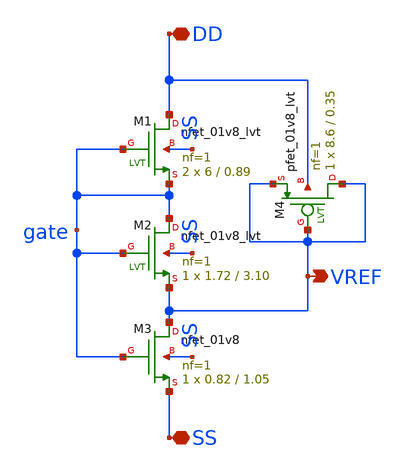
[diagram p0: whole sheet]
** sch_path: xschem/vref01.sch
**.subckt vref01 VREF SS DD
*.opin VREF
*.iopin SS
*.iopin DD
XM1 DD gate gate SS sky130_fd_pr__nfet_01v8_lvt L=0.89 W=6 nf=1 ad='int((nf+1)/2) * W/nf * 0.29' as='int((nf+2)/2) * W/nf * 0.29'
+ pd='2*int((nf+1)/2) * (W/nf + 0.29)' ps='2*int((nf+2)/2) * (W/nf + 0.29)' nrd='0.29 / W' nrs='0.29 / W'
+ sa=0 sb=0 sd=0 mult=2 m=2
XM2 gate gate VREF SS sky130_fd_pr__nfet_01v8_lvt L=3.10 W=1.72 nf=1 ad='int((nf+1)/2) * W/nf * 0.29'
+ as='int((nf+2)/2) * W/nf * 0.29' pd='2*int((nf+1)/2) * (W/nf + 0.29)' ps='2*int((nf+2)/2) * (W/nf + 0.29)'
+ nrd='0.29 / W' nrs='0.29 / W' sa=0 sb=0 sd=0 mult=1 m=1
XM3 VREF gate SS SS sky130_fd_pr__nfet_01v8 L=1.05 W=0.82 nf=1 ad='int((nf+1)/2) * W/nf * 0.29' as='int((nf+2)/2) * W/nf * 0.29'
+ pd='2*int((nf+1)/2) * (W/nf + 0.29)' ps='2*int((nf+2)/2) * (W/nf + 0.29)' nrd='0.29 / W' nrs='0.29 / W'
+ sa=0 sb=0 sd=0 mult=1 m=1
XM4 VREF VREF VREF DD sky130_fd_pr__pfet_01v8_lvt L=0.35 W=8.6 nf=1 ad='int((nf+1)/2) * W/nf * 1' as='int((nf+2)/2) * W/nf * 1'
+ pd='2*int((nf+1)/2) * (W/nf + 1)' ps='2*int((nf+2)/2) * (W/nf + 1)' nrd='1 / W' nrs='1 / W' sa=0 sb=0
+ sd=0 mult=1 m=1
**.ends
.end
